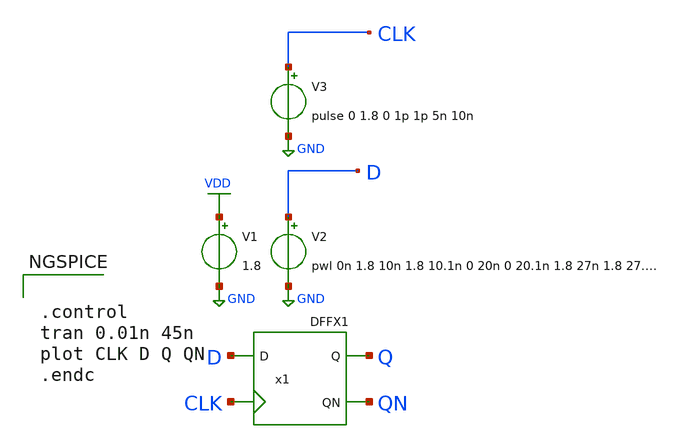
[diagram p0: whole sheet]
** sch_path: lib/xschem/test_TMRDFFQNX1.sch
**.subckt test_TMRDFFQNX1
V2 D GND pwl 0n 1.8 10n 1.8 10.1n 0 20n 0 20.1n 1.8 27n 1.8 27.1n 0 34n 0 34.1n 1.8
V1 VDD GND 1.8
V3 CLK GND pulse 0 1.8 0 1p 1p 5n 10n
x1 Q QN D CLK VDD GND DFFX1
**** begin user architecture code

.lib $::SKYWATER_MODELS/sky130.lib.spice tt


**** end user architecture code
**.ends

* expanding   symbol:  DFFX1.sym # of pins=4
** sym_path: DFFX1.sym
** sch_path: DFFX1.sch
.subckt DFFX1 Q QN D CLK VDD VSS
*.ipin CLK
*.ipin D
*.opin QN
*.opin Q
x1 net2 net3 CLK net1 NAND3X1
x2 net1 net2 D NAND2X1
x3 net4 net1 net3 NAND2X1
x4 net3 net4 CLK NAND2X1
x5 QN net2 Q NAND2X1
x6 Q QN net3 NAND2X1
.ends


* expanding   symbol:  NAND3X1.sym # of pins=4
** sym_path: lib/xschem/NAND3X1.sym
** sch_path: lib/xschem/NAND3X1.sch
.subckt NAND3X1 Y A B C
*.ipin A
*.opin Y
*.ipin B
*.ipin C
XM1 net2 C GND GND sky130_fd_pr__nfet_01v8 L=0.15 W=3 nf=1 ad='int((nf+1)/2) * W/nf * 0.29' as='int((nf+2)/2) * W/nf * 0.29'
+ pd='2*int((nf+1)/2) * (W/nf + 0.29)' ps='2*int((nf+2)/2) * (W/nf + 0.29)' nrd='0.29 / W' nrs='0.29 / W'
+ sa=0 sb=0 sd=0 mult=1 m=1
XM2 Y A VDD VDD sky130_fd_pr__pfet_01v8 L=0.15 W=2 nf=1 ad='int((nf+1)/2) * W/nf * 0.29' as='int((nf+2)/2) * W/nf * 0.29'
+ pd='2*int((nf+1)/2) * (W/nf + 0.29)' ps='2*int((nf+2)/2) * (W/nf + 0.29)' nrd='0.29 / W' nrs='0.29 / W'
+ sa=0 sb=0 sd=0 mult=1 m=1
XM3 net1 B net2 GND sky130_fd_pr__nfet_01v8 L=0.15 W=3 nf=1 ad='int((nf+1)/2) * W/nf * 0.29' as='int((nf+2)/2) * W/nf * 0.29'
+ pd='2*int((nf+1)/2) * (W/nf + 0.29)' ps='2*int((nf+2)/2) * (W/nf + 0.29)' nrd='0.29 / W' nrs='0.29 / W'
+ sa=0 sb=0 sd=0 mult=1 m=1
XM4 Y A net1 GND sky130_fd_pr__nfet_01v8 L=0.15 W=3 nf=1 ad='int((nf+1)/2) * W/nf * 0.29' as='int((nf+2)/2) * W/nf * 0.29'
+ pd='2*int((nf+1)/2) * (W/nf + 0.29)' ps='2*int((nf+2)/2) * (W/nf + 0.29)' nrd='0.29 / W' nrs='0.29 / W'
+ sa=0 sb=0 sd=0 mult=1 m=1
XM5 Y A VDD VDD sky130_fd_pr__pfet_01v8 L=0.15 W=2 nf=1 ad='int((nf+1)/2) * W/nf * 0.29' as='int((nf+2)/2) * W/nf * 0.29'
+ pd='2*int((nf+1)/2) * (W/nf + 0.29)' ps='2*int((nf+2)/2) * (W/nf + 0.29)' nrd='0.29 / W' nrs='0.29 / W'
+ sa=0 sb=0 sd=0 mult=1 m=1
XM6 Y B VDD VDD sky130_fd_pr__pfet_01v8 L=0.15 W=2 nf=1 ad='int((nf+1)/2) * W/nf * 0.29' as='int((nf+2)/2) * W/nf * 0.29'
+ pd='2*int((nf+1)/2) * (W/nf + 0.29)' ps='2*int((nf+2)/2) * (W/nf + 0.29)' nrd='0.29 / W' nrs='0.29 / W'
+ sa=0 sb=0 sd=0 mult=1 m=1
XM7 Y B VDD VDD sky130_fd_pr__pfet_01v8 L=0.15 W=2 nf=1 ad='int((nf+1)/2) * W/nf * 0.29' as='int((nf+2)/2) * W/nf * 0.29'
+ pd='2*int((nf+1)/2) * (W/nf + 0.29)' ps='2*int((nf+2)/2) * (W/nf + 0.29)' nrd='0.29 / W' nrs='0.29 / W'
+ sa=0 sb=0 sd=0 mult=1 m=1
XM8 Y C VDD VDD sky130_fd_pr__pfet_01v8 L=0.15 W=2 nf=1 ad='int((nf+1)/2) * W/nf * 0.29' as='int((nf+2)/2) * W/nf * 0.29'
+ pd='2*int((nf+1)/2) * (W/nf + 0.29)' ps='2*int((nf+2)/2) * (W/nf + 0.29)' nrd='0.29 / W' nrs='0.29 / W'
+ sa=0 sb=0 sd=0 mult=1 m=1
XM9 Y C VDD VDD sky130_fd_pr__pfet_01v8 L=0.15 W=2 nf=1 ad='int((nf+1)/2) * W/nf * 0.29' as='int((nf+2)/2) * W/nf * 0.29'
+ pd='2*int((nf+1)/2) * (W/nf + 0.29)' ps='2*int((nf+2)/2) * (W/nf + 0.29)' nrd='0.29 / W' nrs='0.29 / W'
+ sa=0 sb=0 sd=0 mult=1 m=1
.ends


* expanding   symbol:  NAND2X1.sym # of pins=3
** sym_path: lib/xschem/NAND2X1.sym
** sch_path: lib/xschem/NAND2X1.sch
.subckt NAND2X1 Y A B
*.ipin A
*.opin Y
*.ipin B
XM1 Y A VDD VDD sky130_fd_pr__pfet_01v8 L=0.15 W=2 nf=1 ad='int((nf+1)/2) * W/nf * 0.29' as='int((nf+2)/2) * W/nf * 0.29'
+ pd='2*int((nf+1)/2) * (W/nf + 0.29)' ps='2*int((nf+2)/2) * (W/nf + 0.29)' nrd='0.29 / W' nrs='0.29 / W'
+ sa=0 sb=0 sd=0 mult=1 m=1
XM5 Y A net1 VSS sky130_fd_pr__nfet_01v8 L=0.15 W=3 nf=1 ad='int((nf+1)/2) * W/nf * 0.29' as='int((nf+2)/2) * W/nf * 0.29'
+ pd='2*int((nf+1)/2) * (W/nf + 0.29)' ps='2*int((nf+2)/2) * (W/nf + 0.29)' nrd='0.29 / W' nrs='0.29 / W'
+ sa=0 sb=0 sd=0 mult=1 m=1
XM2 Y A VDD VDD sky130_fd_pr__pfet_01v8 L=0.15 W=2 nf=1 ad='int((nf+1)/2) * W/nf * 0.29' as='int((nf+2)/2) * W/nf * 0.29'
+ pd='2*int((nf+1)/2) * (W/nf + 0.29)' ps='2*int((nf+2)/2) * (W/nf + 0.29)' nrd='0.29 / W' nrs='0.29 / W'
+ sa=0 sb=0 sd=0 mult=1 m=1
XM3 Y B VDD VDD sky130_fd_pr__pfet_01v8 L=0.15 W=2 nf=1 ad='int((nf+1)/2) * W/nf * 0.29' as='int((nf+2)/2) * W/nf * 0.29'
+ pd='2*int((nf+1)/2) * (W/nf + 0.29)' ps='2*int((nf+2)/2) * (W/nf + 0.29)' nrd='0.29 / W' nrs='0.29 / W'
+ sa=0 sb=0 sd=0 mult=1 m=1
XM4 Y B VDD VDD sky130_fd_pr__pfet_01v8 L=0.15 W=2 nf=1 ad='int((nf+1)/2) * W/nf * 0.29' as='int((nf+2)/2) * W/nf * 0.29'
+ pd='2*int((nf+1)/2) * (W/nf + 0.29)' ps='2*int((nf+2)/2) * (W/nf + 0.29)' nrd='0.29 / W' nrs='0.29 / W'
+ sa=0 sb=0 sd=0 mult=1 m=1
XM6 net1 B VSS VSS sky130_fd_pr__nfet_01v8 L=0.15 W=3 nf=1 ad='int((nf+1)/2) * W/nf * 0.29' as='int((nf+2)/2) * W/nf * 0.29'
+ pd='2*int((nf+1)/2) * (W/nf + 0.29)' ps='2*int((nf+2)/2) * (W/nf + 0.29)' nrd='0.29 / W' nrs='0.29 / W'
+ sa=0 sb=0 sd=0 mult=1 m=1
.ends

.GLOBAL VDD
.GLOBAL GND
**** begin user architecture code


.control
tran 0.01n 45n
plot CLK D Q QN
.endc


**** end user architecture code
.end
